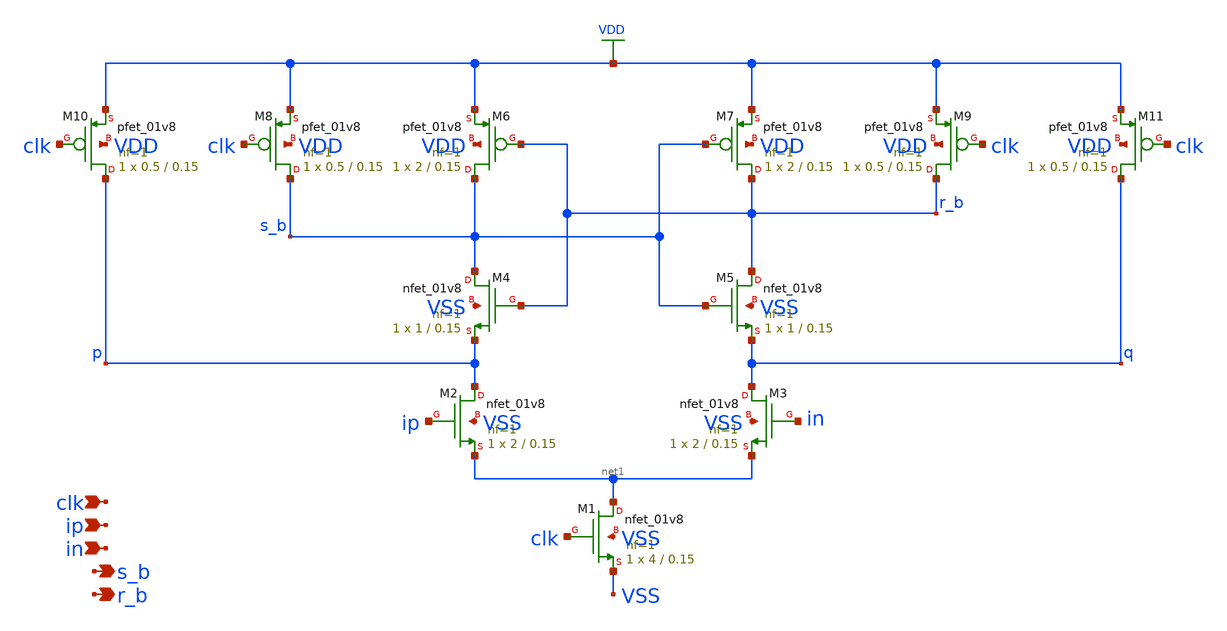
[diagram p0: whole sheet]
** sch_path: design/analog_modulator/schematic/comparator_core_small.sch
**.subckt comparator_core_small clk ip in s_b r_b
*.ipin clk
*.ipin ip
*.ipin in
*.opin s_b
*.opin r_b
XM1 net1 clk VSS VSS sky130_fd_pr__nfet_01v8 L=0.15 W=4 nf=1 ad='int((nf+1)/2) * W/nf * 0.29' as='int((nf+2)/2) * W/nf * 0.29'
+ pd='2*int((nf+1)/2) * (W/nf + 0.29)' ps='2*int((nf+2)/2) * (W/nf + 0.29)' nrd='0.29 / W' nrs='0.29 / W'
+ sa=0 sb=0 sd=0 mult=1 m=1
XM2 p ip net1 VSS sky130_fd_pr__nfet_01v8 L=0.15 W=2 nf=1 ad='int((nf+1)/2) * W/nf * 0.29' as='int((nf+2)/2) * W/nf * 0.29'
+ pd='2*int((nf+1)/2) * (W/nf + 0.29)' ps='2*int((nf+2)/2) * (W/nf + 0.29)' nrd='0.29 / W' nrs='0.29 / W'
+ sa=0 sb=0 sd=0 mult=1 m=1
XM3 q in net1 VSS sky130_fd_pr__nfet_01v8 L=0.15 W=2 nf=1 ad='int((nf+1)/2) * W/nf * 0.29' as='int((nf+2)/2) * W/nf * 0.29'
+ pd='2*int((nf+1)/2) * (W/nf + 0.29)' ps='2*int((nf+2)/2) * (W/nf + 0.29)' nrd='0.29 / W' nrs='0.29 / W'
+ sa=0 sb=0 sd=0 mult=1 m=1
XM4 s_b r_b p VSS sky130_fd_pr__nfet_01v8 L=0.15 W=1 nf=1 ad='int((nf+1)/2) * W/nf * 0.29' as='int((nf+2)/2) * W/nf * 0.29'
+ pd='2*int((nf+1)/2) * (W/nf + 0.29)' ps='2*int((nf+2)/2) * (W/nf + 0.29)' nrd='0.29 / W' nrs='0.29 / W'
+ sa=0 sb=0 sd=0 mult=1 m=1
XM5 r_b s_b q VSS sky130_fd_pr__nfet_01v8 L=0.15 W=1 nf=1 ad='int((nf+1)/2) * W/nf * 0.29' as='int((nf+2)/2) * W/nf * 0.29'
+ pd='2*int((nf+1)/2) * (W/nf + 0.29)' ps='2*int((nf+2)/2) * (W/nf + 0.29)' nrd='0.29 / W' nrs='0.29 / W'
+ sa=0 sb=0 sd=0 mult=1 m=1
XM6 s_b r_b VDD VDD sky130_fd_pr__pfet_01v8 L=0.15 W=2 nf=1 ad='int((nf+1)/2) * W/nf * 0.29' as='int((nf+2)/2) * W/nf * 0.29'
+ pd='2*int((nf+1)/2) * (W/nf + 0.29)' ps='2*int((nf+2)/2) * (W/nf + 0.29)' nrd='0.29 / W' nrs='0.29 / W'
+ sa=0 sb=0 sd=0 mult=1 m=1
XM7 r_b s_b VDD VDD sky130_fd_pr__pfet_01v8 L=0.15 W=2 nf=1 ad='int((nf+1)/2) * W/nf * 0.29' as='int((nf+2)/2) * W/nf * 0.29'
+ pd='2*int((nf+1)/2) * (W/nf + 0.29)' ps='2*int((nf+2)/2) * (W/nf + 0.29)' nrd='0.29 / W' nrs='0.29 / W'
+ sa=0 sb=0 sd=0 mult=1 m=1
XM8 s_b clk VDD VDD sky130_fd_pr__pfet_01v8 L=0.15 W=0.5 nf=1 ad='int((nf+1)/2) * W/nf * 0.29' as='int((nf+2)/2) * W/nf * 0.29'
+ pd='2*int((nf+1)/2) * (W/nf + 0.29)' ps='2*int((nf+2)/2) * (W/nf + 0.29)' nrd='0.29 / W' nrs='0.29 / W'
+ sa=0 sb=0 sd=0 mult=1 m=1
XM9 r_b clk VDD VDD sky130_fd_pr__pfet_01v8 L=0.15 W=0.5 nf=1 ad='int((nf+1)/2) * W/nf * 0.29' as='int((nf+2)/2) * W/nf * 0.29'
+ pd='2*int((nf+1)/2) * (W/nf + 0.29)' ps='2*int((nf+2)/2) * (W/nf + 0.29)' nrd='0.29 / W' nrs='0.29 / W'
+ sa=0 sb=0 sd=0 mult=1 m=1
XM10 p clk VDD VDD sky130_fd_pr__pfet_01v8 L=0.15 W=0.5 nf=1 ad='int((nf+1)/2) * W/nf * 0.29' as='int((nf+2)/2) * W/nf * 0.29'
+ pd='2*int((nf+1)/2) * (W/nf + 0.29)' ps='2*int((nf+2)/2) * (W/nf + 0.29)' nrd='0.29 / W' nrs='0.29 / W'
+ sa=0 sb=0 sd=0 mult=1 m=1
XM11 q clk VDD VDD sky130_fd_pr__pfet_01v8 L=0.15 W=0.5 nf=1 ad='int((nf+1)/2) * W/nf * 0.29' as='int((nf+2)/2) * W/nf * 0.29'
+ pd='2*int((nf+1)/2) * (W/nf + 0.29)' ps='2*int((nf+2)/2) * (W/nf + 0.29)' nrd='0.29 / W' nrs='0.29 / W'
+ sa=0 sb=0 sd=0 mult=1 m=1
**.ends
.GLOBAL VDD
.end
